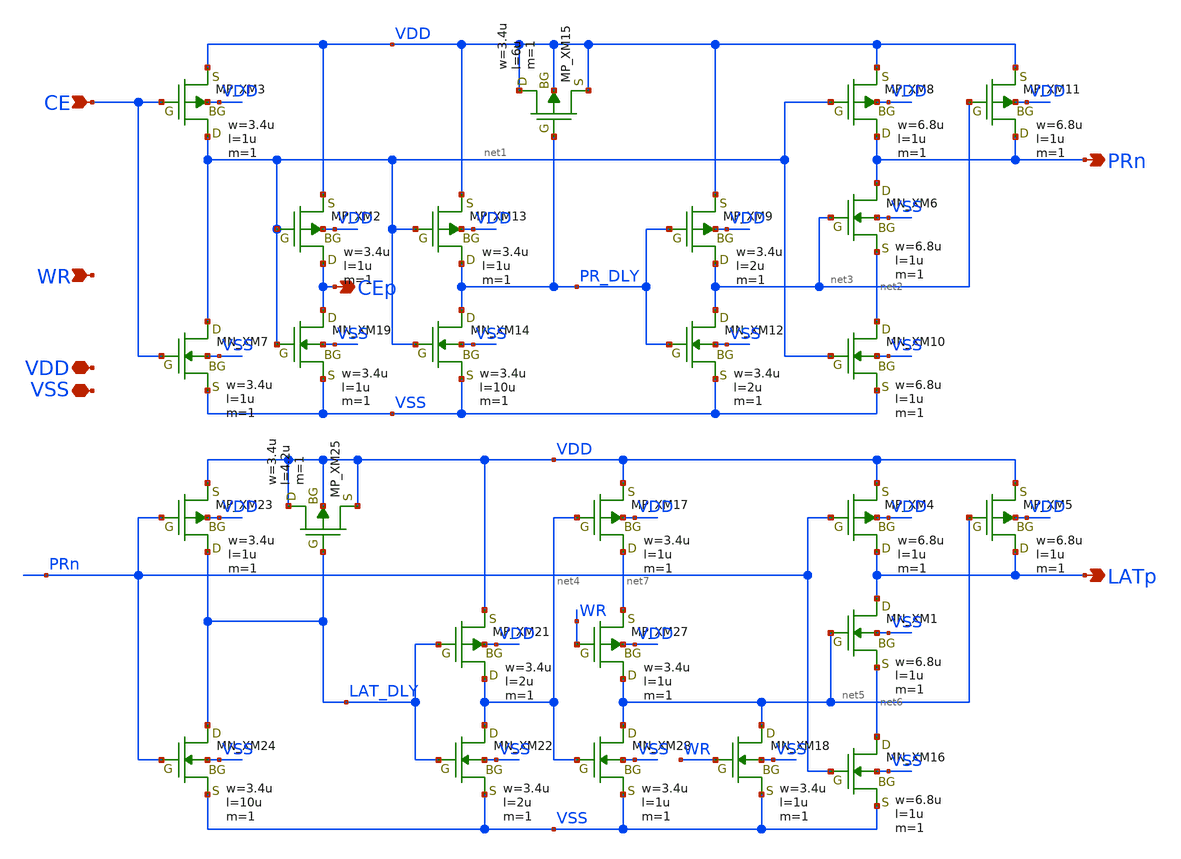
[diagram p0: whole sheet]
** sch_path: module/SRAM128/schematic/SACTR.sch
**.subckt SACTR PRn CE VDD VSS LATp WR CEp
*.opin PRn
*.ipin CE
*.iopin VDD
*.iopin VSS
*.opin LATp
*.ipin WR
*.opin CEp
XXM3 net1 CE VDD VDD PMOS w=3.4u l=1u as=0 ad=0 ps=0 pd=0 nrd=0 nrs=0 m=1
XXM7 net1 CE VSS VSS NMOS w=3.4u l=1u as=0 ad=0 ps=0 pd=0 nrd=0 nrs=0 m=1
XXM6 PRn net3 net2 VSS NMOS w=6.8u l=1u as=0 ad=0 ps=0 pd=0 nrd=0 nrs=0 m=1
XXM8 PRn net1 VDD VDD PMOS w=6.8u l=1u as=0 ad=0 ps=0 pd=0 nrd=0 nrs=0 m=1
XXM10 net2 net1 VSS VSS NMOS w=6.8u l=1u as=0 ad=0 ps=0 pd=0 nrd=0 nrs=0 m=1
XXM11 PRn net3 VDD VDD PMOS w=6.8u l=1u as=0 ad=0 ps=0 pd=0 nrd=0 nrs=0 m=1
XXM9 net3 PR_DLY VDD VDD PMOS w=3.4u l=2u as=0 ad=0 ps=0 pd=0 nrd=0 nrs=0 m=1
XXM12 net3 PR_DLY VSS VSS NMOS w=3.4u l=2u as=0 ad=0 ps=0 pd=0 nrd=0 nrs=0 m=1
XXM13 PR_DLY net1 VDD VDD PMOS w=3.4u l=1u as=0 ad=0 ps=0 pd=0 nrd=0 nrs=0 m=1
XXM14 PR_DLY net1 VSS VSS NMOS w=3.4u l=10u as=0 ad=0 ps=0 pd=0 nrd=0 nrs=0 m=1
XXM15 VDD PR_DLY VDD VDD PMOS w=3.4u l=6u as=0 ad=0 ps=0 pd=0 nrd=0 nrs=0 m=1
XXM1 LATp net5 net6 VSS NMOS w=6.8u l=1u as=0 ad=0 ps=0 pd=0 nrd=0 nrs=0 m=1
XXM4 LATp PRn VDD VDD PMOS w=6.8u l=1u as=0 ad=0 ps=0 pd=0 nrd=0 nrs=0 m=1
XXM16 net6 PRn VSS VSS NMOS w=6.8u l=1u as=0 ad=0 ps=0 pd=0 nrd=0 nrs=0 m=1
XXM21 net4 LAT_DLY VDD VDD PMOS w=3.4u l=2u as=0 ad=0 ps=0 pd=0 nrd=0 nrs=0 m=1
XXM22 net4 LAT_DLY VSS VSS NMOS w=3.4u l=2u as=0 ad=0 ps=0 pd=0 nrd=0 nrs=0 m=1
XXM23 LAT_DLY PRn VDD VDD PMOS w=3.4u l=1u as=0 ad=0 ps=0 pd=0 nrd=0 nrs=0 m=1
XXM24 LAT_DLY PRn VSS VSS NMOS w=3.4u l=10u as=0 ad=0 ps=0 pd=0 nrd=0 nrs=0 m=1
XXM25 VDD LAT_DLY VDD VDD PMOS w=3.4u l=4.2u as=0 ad=0 ps=0 pd=0 nrd=0 nrs=0 m=1
XXM27 net5 WR net7 VDD PMOS w=3.4u l=1u as=0 ad=0 ps=0 pd=0 nrd=0 nrs=0 m=1
XXM28 net5 net4 VSS VSS NMOS w=3.4u l=1u as=0 ad=0 ps=0 pd=0 nrd=0 nrs=0 m=1
XXM17 net7 net4 VDD VDD PMOS w=3.4u l=1u as=0 ad=0 ps=0 pd=0 nrd=0 nrs=0 m=1
XXM18 net5 WR VSS VSS NMOS w=3.4u l=1u as=0 ad=0 ps=0 pd=0 nrd=0 nrs=0 m=1
XXM5 LATp net5 VDD VDD PMOS w=6.8u l=1u as=0 ad=0 ps=0 pd=0 nrd=0 nrs=0 m=1
XXM2 CEp net1 VDD VDD PMOS w=3.4u l=1u as=0 ad=0 ps=0 pd=0 nrd=0 nrs=0 m=1
XXM19 CEp net1 VSS VSS NMOS w=3.4u l=1u as=0 ad=0 ps=0 pd=0 nrd=0 nrs=0 m=1
**.ends
.end
